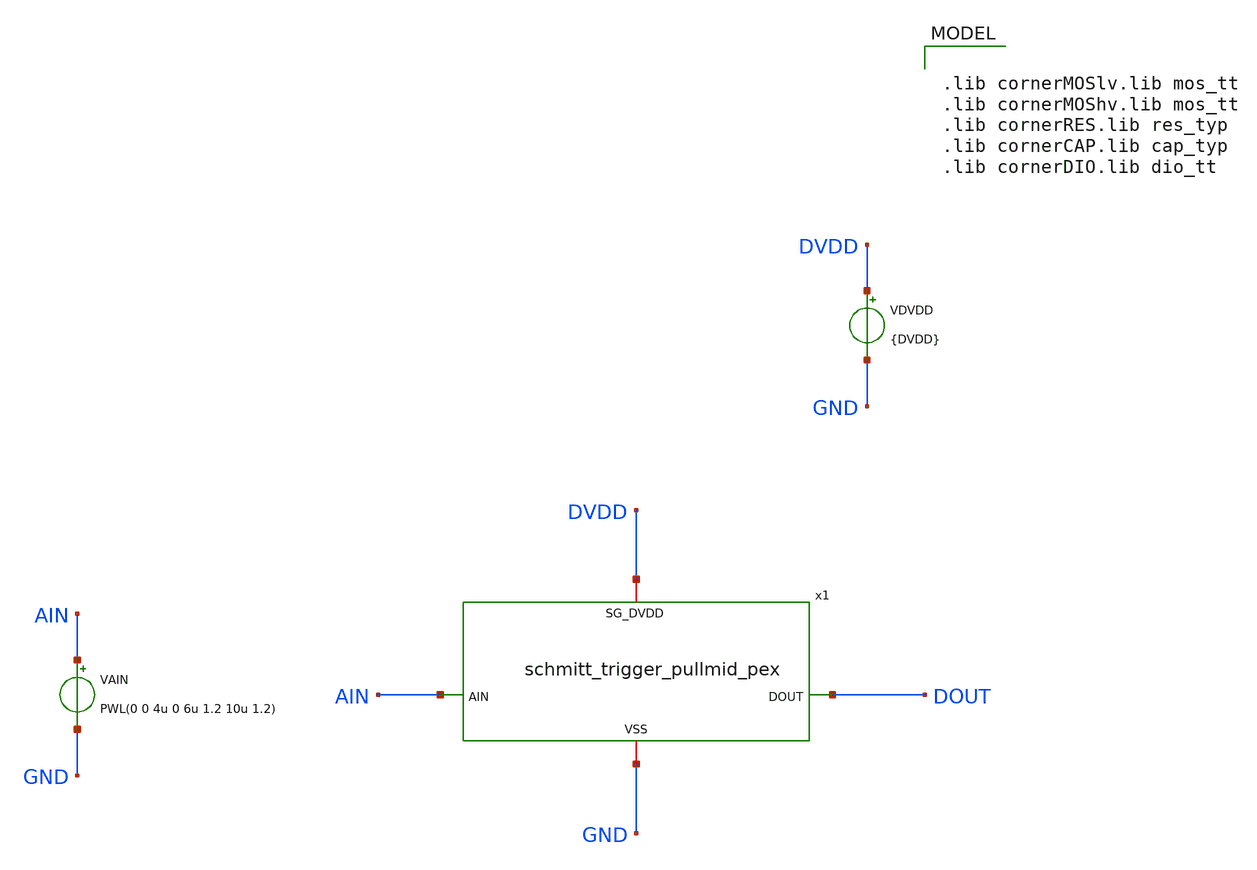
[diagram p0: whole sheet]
** sch_path: macros/schmitt_trigger_pullmid/testbenches/xschem/schmitt_trigger_pullmid_tb_dc_pex.sch
**.subckt schmitt_trigger_pullmid_tb_dc_pex
x1 DVDD AIN DOUT GND schmitt_trigger_pullmid_pex
VAIN AIN GND PWL(0 0 4u 0 6u 1.2 10u 1.2)
VDVDD DVDD GND {DVDD}
**** begin user architecture code


.include ../../../netlist/pex/schmitt_trigger_pullmid_magic_pex_3.spice
.param DVDD=1.2
.csparam DVDD=DVDD
.temp 27
.options savecurrents klu method=gear reltol=1e-3 abstol=1e-12 gmin=1e-12
.control

save all

tran 100p 10u
write @schname\.raw

plot ain dout

unset appendwrite
set wr_vecnames
set wr_singlescale
wrdata ../plot_simulations/data/@schname\.txt v(ain) v(dout)

*quit
.endc



.lib cornerMOSlv.lib mos_tt
.lib cornerMOShv.lib mos_tt
.lib cornerRES.lib res_typ
.lib cornerCAP.lib cap_typ
.lib cornerDIO.lib dio_tt

**** end user architecture code
**.ends
.end
